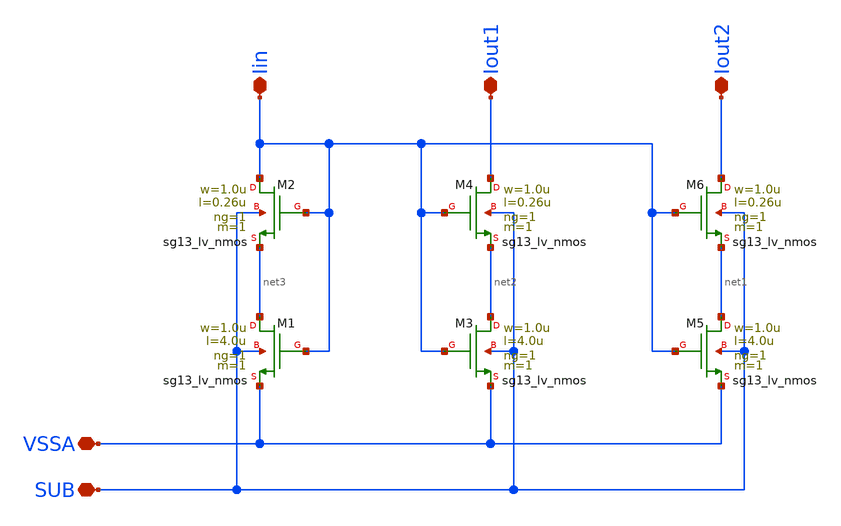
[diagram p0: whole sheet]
** sch_path: xschem/Nmirror.sch
**.subckt Nmirror VSSA SUB Iin Iout1 Iout2
*.iopin VSSA
*.iopin SUB
*.iopin Iin
*.iopin Iout1
*.iopin Iout2
XM1 net3 Iin VSSA SUB sg13_lv_nmos w=1.0u l=4.0u ng=1 m=1 mm_ok=1
XM3 net2 Iin VSSA SUB sg13_lv_nmos w=1.0u l=4.0u ng=1 m=1 mm_ok=1
XM2 Iin Iin net3 SUB sg13_lv_nmos w=1.0u l=0.26u ng=1 m=1 mm_ok=1
XM4 Iout1 Iin net2 SUB sg13_lv_nmos w=1.0u l=0.26u ng=1 m=1 mm_ok=1
XM5 net1 Iin VSSA SUB sg13_lv_nmos w=1.0u l=4.0u ng=1 m=1 mm_ok=1
XM6 Iout2 Iin net1 SUB sg13_lv_nmos w=1.0u l=0.26u ng=1 m=1 mm_ok=1
**.ends
.end
